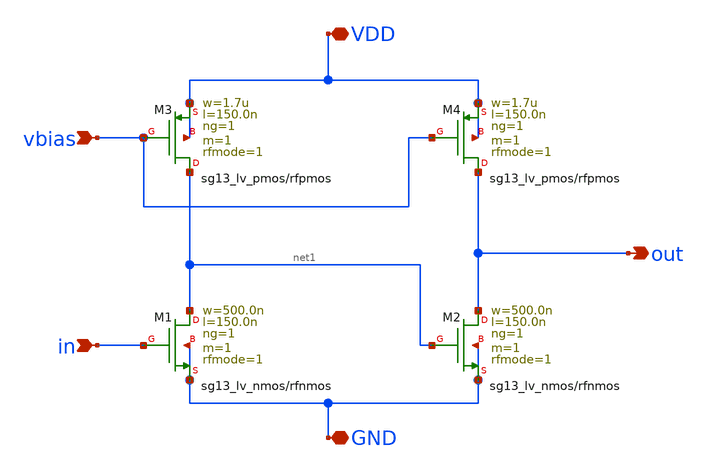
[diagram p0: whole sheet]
** sch_path: UWBPulseGenerator/design_data/xschem/inverter_pseudo.sch
**.subckt inverter_pseudo vbias in out VDD GND
*.ipin vbias
*.ipin in
*.opin out
*.iopin VDD
*.iopin GND
XM1 net1 in GND GND sg13_lv_nmos w=500.0n l=150.0n ng=1 m=1 rfmode=1 mm_ok=1
XM3 net1 vbias VDD VDD sg13_lv_pmos w=1.7u l=150.0n ng=1 m=1 rfmode=1 mm_ok=1
XM2 out net1 GND GND sg13_lv_nmos w=500.0n l=150.0n ng=1 m=1 rfmode=1 mm_ok=1
XM4 out vbias VDD VDD sg13_lv_pmos w=1.7u l=150.0n ng=1 m=1 rfmode=1 mm_ok=1
**.ends
.end
